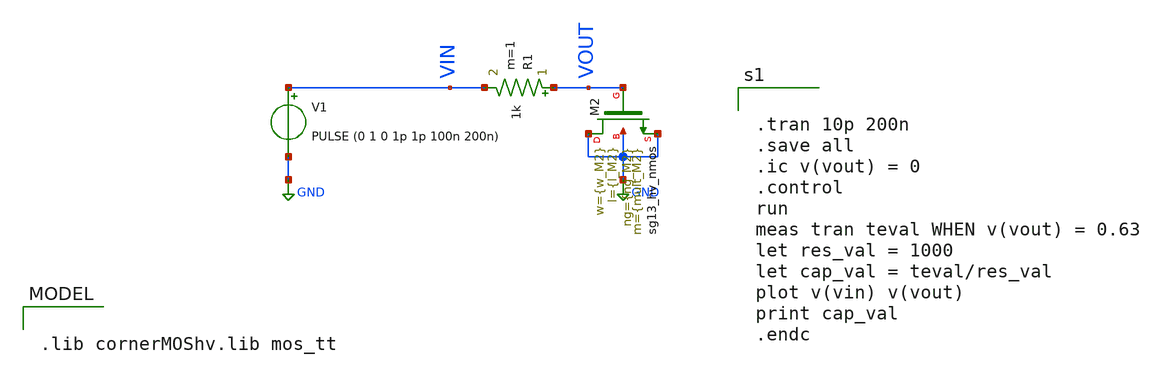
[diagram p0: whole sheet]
** sch_path: xschem/TB_hvNMOS_cgate-ext.sch
**.subckt TB_hvNMOS_cgate-ext
R1 VOUT VIN 1k m=1
V1 VIN GND PULSE (0 1 0 1p 1p 100n 200n)
XM2 GND VOUT GND GND sg13_hv_nmos w={w_M2} l={l_M2} ng={ng_M2} m={mult_M2} mm_ok=1
**** begin user architecture code


.tran 10p 200n
.save all
.ic v(vout) = 0
.control
run
meas tran teval WHEN v(vout) = 0.63
let res_val = 1000
let cap_val = teval/res_val
plot v(vin) v(vout)
print cap_val
.endc




.param temp=27

.param mult_M2 = 1200
.param w_M2 =10u
*.param l_M2 =0.25u
.param l_M2 =0.25u
.param ng_M2 =1






.lib cornerMOShv.lib mos_tt

**** end user architecture code
**.ends
.GLOBAL GND
.end
